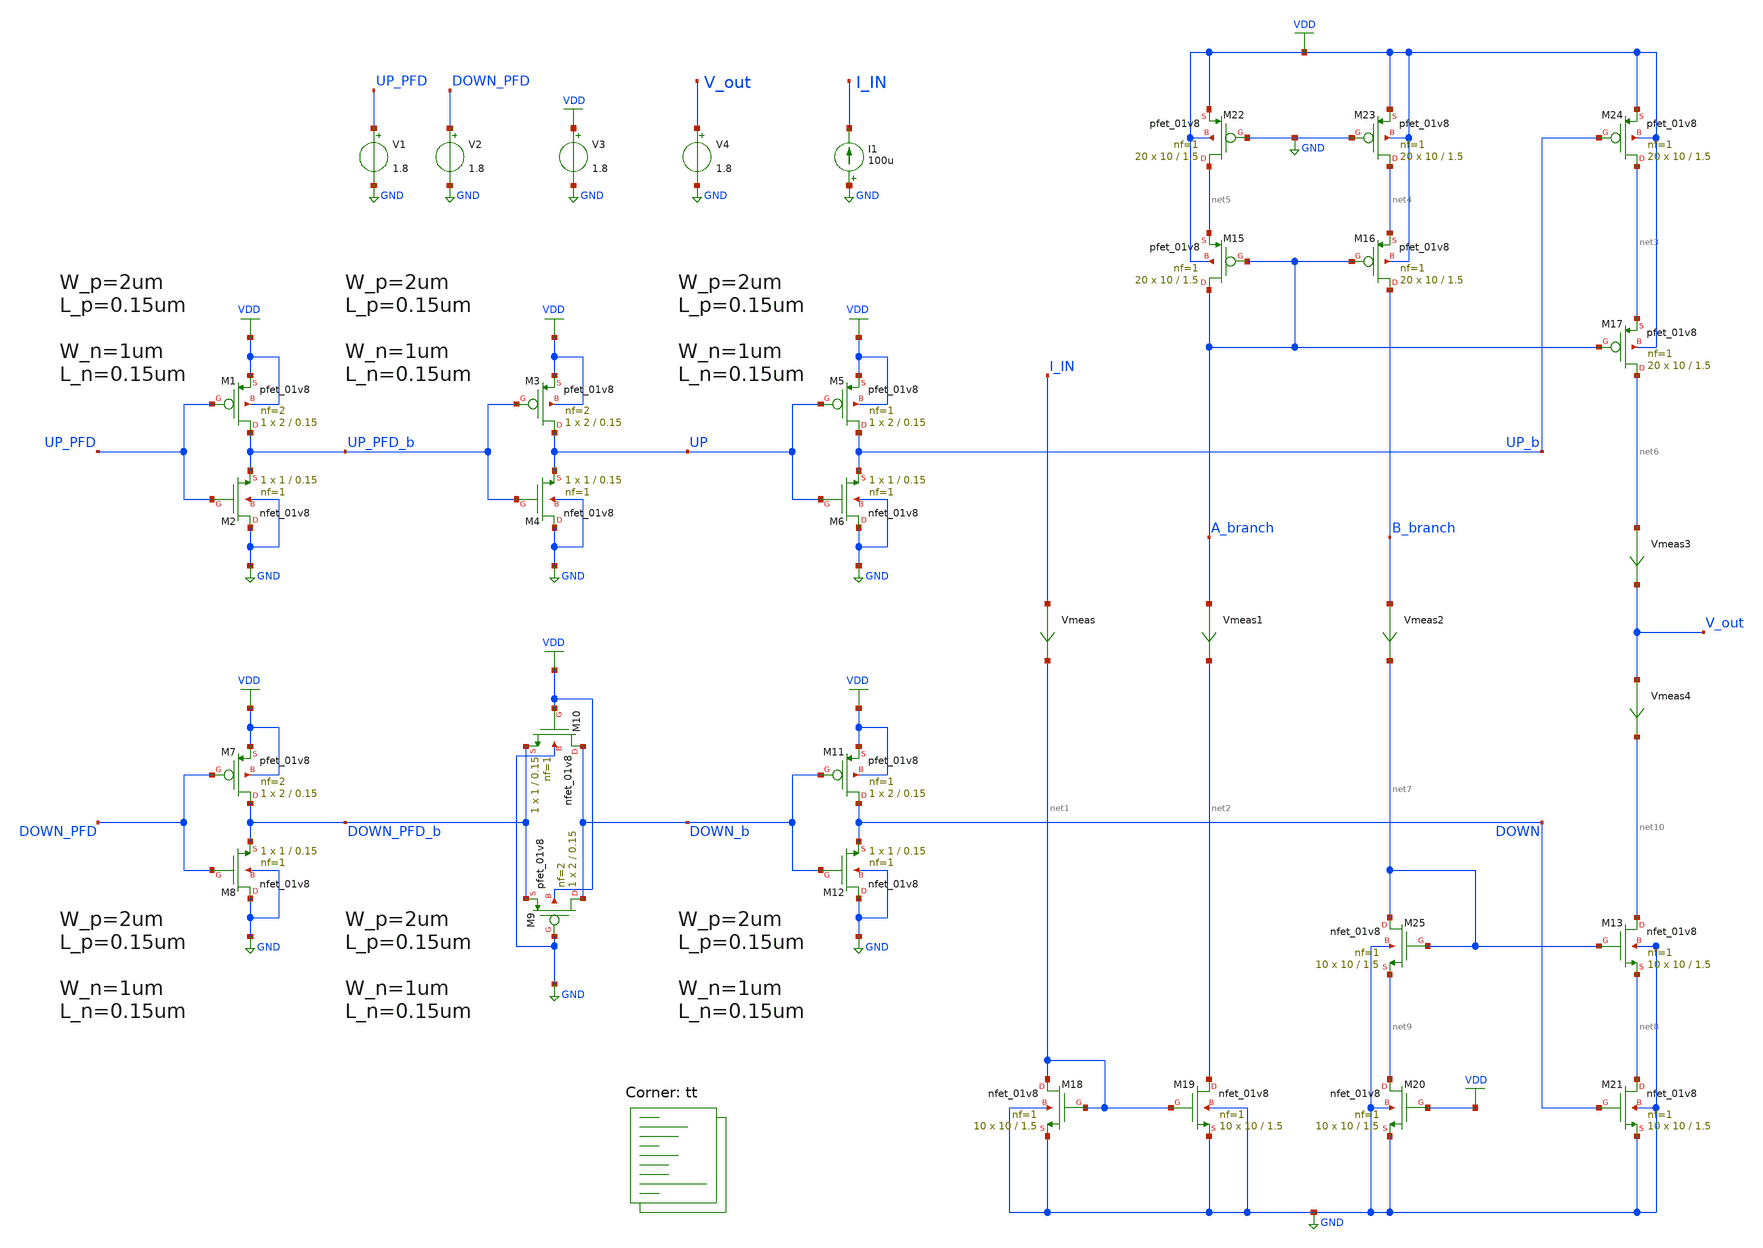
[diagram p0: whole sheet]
** sch_path: projects/pll/charge_pump/xschem_ngspice/charge_pump_DC11.sch
**.subckt charge_pump_DC11
XM9 DOWN_b GND DOWN_PFD_b VDD sky130_fd_pr__pfet_01v8 L=0.15 W=2 nf=2 ad='int((nf+1)/2) * W/nf * 0.29'
+ as='int((nf+2)/2) * W/nf * 0.29' pd='2*int((nf+1)/2) * (W/nf + 0.29)' ps='2*int((nf+2)/2) * (W/nf + 0.29)'
+ nrd='0.29 / W' nrs='0.29 / W' sa=0 sb=0 sd=0 mult=1 m=1
XM10 DOWN_b VDD DOWN_PFD_b GND sky130_fd_pr__nfet_01v8 L=0.15 W=1 nf=1 ad='int((nf+1)/2) * W/nf * 0.29'
+ as='int((nf+2)/2) * W/nf * 0.29' pd='2*int((nf+1)/2) * (W/nf + 0.29)' ps='2*int((nf+2)/2) * (W/nf + 0.29)'
+ nrd='0.29 / W' nrs='0.29 / W' sa=0 sb=0 sd=0 mult=1 m=1
XM1 UP_PFD_b UP_PFD VDD VDD sky130_fd_pr__pfet_01v8 L=0.15 W=2 nf=2 ad='int((nf+1)/2) * W/nf * 0.29'
+ as='int((nf+2)/2) * W/nf * 0.29' pd='2*int((nf+1)/2) * (W/nf + 0.29)' ps='2*int((nf+2)/2) * (W/nf + 0.29)'
+ nrd='0.29 / W' nrs='0.29 / W' sa=0 sb=0 sd=0 mult=1 m=1
XM2 GND UP_PFD UP_PFD_b GND sky130_fd_pr__nfet_01v8 L=0.15 W=1 nf=1 ad='int((nf+1)/2) * W/nf * 0.29'
+ as='int((nf+2)/2) * W/nf * 0.29' pd='2*int((nf+1)/2) * (W/nf + 0.29)' ps='2*int((nf+2)/2) * (W/nf + 0.29)'
+ nrd='0.29 / W' nrs='0.29 / W' sa=0 sb=0 sd=0 mult=1 m=1
XM7 DOWN_PFD_b DOWN_PFD VDD VDD sky130_fd_pr__pfet_01v8 L=0.15 W=2 nf=2 ad='int((nf+1)/2) * W/nf * 0.29'
+ as='int((nf+2)/2) * W/nf * 0.29' pd='2*int((nf+1)/2) * (W/nf + 0.29)' ps='2*int((nf+2)/2) * (W/nf + 0.29)'
+ nrd='0.29 / W' nrs='0.29 / W' sa=0 sb=0 sd=0 mult=1 m=1
XM8 GND DOWN_PFD DOWN_PFD_b GND sky130_fd_pr__nfet_01v8 L=0.15 W=1 nf=1 ad='int((nf+1)/2) * W/nf * 0.29'
+ as='int((nf+2)/2) * W/nf * 0.29' pd='2*int((nf+1)/2) * (W/nf + 0.29)' ps='2*int((nf+2)/2) * (W/nf + 0.29)'
+ nrd='0.29 / W' nrs='0.29 / W' sa=0 sb=0 sd=0 mult=1 m=1
XM3 UP UP_PFD_b VDD VDD sky130_fd_pr__pfet_01v8 L=0.15 W=2 nf=2 ad='int((nf+1)/2) * W/nf * 0.29' as='int((nf+2)/2) * W/nf * 0.29'
+ pd='2*int((nf+1)/2) * (W/nf + 0.29)' ps='2*int((nf+2)/2) * (W/nf + 0.29)' nrd='0.29 / W' nrs='0.29 / W'
+ sa=0 sb=0 sd=0 mult=1 m=1
XM4 GND UP_PFD_b UP GND sky130_fd_pr__nfet_01v8 L=0.15 W=1 nf=1 ad='int((nf+1)/2) * W/nf * 0.29' as='int((nf+2)/2) * W/nf * 0.29'
+ pd='2*int((nf+1)/2) * (W/nf + 0.29)' ps='2*int((nf+2)/2) * (W/nf + 0.29)' nrd='0.29 / W' nrs='0.29 / W'
+ sa=0 sb=0 sd=0 mult=1 m=1
V3 VDD GND 1.8
I1 GND I_IN 100u
V1 UP_PFD GND 1.8
V2 DOWN_PFD GND 1.8
V4 V_out GND 1.8
XM5 UP_b UP VDD VDD sky130_fd_pr__pfet_01v8 L=0.15 W=2 nf=1 ad='int((nf+1)/2) * W/nf * 0.29' as='int((nf+2)/2) * W/nf * 0.29'
+ pd='2*int((nf+1)/2) * (W/nf + 0.29)' ps='2*int((nf+2)/2) * (W/nf + 0.29)' nrd='0.29 / W' nrs='0.29 / W'
+ sa=0 sb=0 sd=0 mult=1 m=1
XM6 GND UP UP_b GND sky130_fd_pr__nfet_01v8 L=0.15 W=1 nf=1 ad='int((nf+1)/2) * W/nf * 0.29' as='int((nf+2)/2) * W/nf * 0.29'
+ pd='2*int((nf+1)/2) * (W/nf + 0.29)' ps='2*int((nf+2)/2) * (W/nf + 0.29)' nrd='0.29 / W' nrs='0.29 / W'
+ sa=0 sb=0 sd=0 mult=1 m=1
XM11 DOWN DOWN_b VDD VDD sky130_fd_pr__pfet_01v8 L=0.15 W=2 nf=1 ad='int((nf+1)/2) * W/nf * 0.29' as='int((nf+2)/2) * W/nf * 0.29'
+ pd='2*int((nf+1)/2) * (W/nf + 0.29)' ps='2*int((nf+2)/2) * (W/nf + 0.29)' nrd='0.29 / W' nrs='0.29 / W'
+ sa=0 sb=0 sd=0 mult=1 m=1
XM12 GND DOWN_b DOWN GND sky130_fd_pr__nfet_01v8 L=0.15 W=1 nf=1 ad='int((nf+1)/2) * W/nf * 0.29' as='int((nf+2)/2) * W/nf * 0.29'
+ pd='2*int((nf+1)/2) * (W/nf + 0.29)' ps='2*int((nf+2)/2) * (W/nf + 0.29)' nrd='0.29 / W' nrs='0.29 / W'
+ sa=0 sb=0 sd=0 mult=1 m=1
XM18 net1 net1 GND GND sky130_fd_pr__nfet_01v8 L=1.5 W=10 nf=1 ad='int((nf+1)/2) * W/nf * 0.29' as='int((nf+2)/2) * W/nf * 0.29'
+ pd='2*int((nf+1)/2) * (W/nf + 0.29)' ps='2*int((nf+2)/2) * (W/nf + 0.29)' nrd='0.29 / W' nrs='0.29 / W'
+ sa=0 sb=0 sd=0 mult=10 m=10
XM19 net2 net1 GND GND sky130_fd_pr__nfet_01v8 L=1.5 W=10 nf=1 ad='int((nf+1)/2) * W/nf * 0.29' as='int((nf+2)/2) * W/nf * 0.29'
+ pd='2*int((nf+1)/2) * (W/nf + 0.29)' ps='2*int((nf+2)/2) * (W/nf + 0.29)' nrd='0.29 / W' nrs='0.29 / W'
+ sa=0 sb=0 sd=0 mult=10 m=10
Vmeas I_IN net1 0
.save i(vmeas)
Vmeas3 net6 V_out 0
.save i(vmeas3)
Vmeas4 V_out net10 0
.save i(vmeas4)
XM17 net6 A_branch net3 VDD sky130_fd_pr__pfet_01v8 L=1.5 W=10 nf=1 ad='int((nf+1)/2) * W/nf * 0.29'
+ as='int((nf+2)/2) * W/nf * 0.29' pd='2*int((nf+1)/2) * (W/nf + 0.29)' ps='2*int((nf+2)/2) * (W/nf + 0.29)'
+ nrd='0.29 / W' nrs='0.29 / W' sa=0 sb=0 sd=0 mult=20 m=20
XM21 net8 DOWN GND GND sky130_fd_pr__nfet_01v8 L=1.5 W=10 nf=1 ad='int((nf+1)/2) * W/nf * 0.29' as='int((nf+2)/2) * W/nf * 0.29'
+ pd='2*int((nf+1)/2) * (W/nf + 0.29)' ps='2*int((nf+2)/2) * (W/nf + 0.29)' nrd='0.29 / W' nrs='0.29 / W'
+ sa=0 sb=0 sd=0 mult=10 m=10
XM20 net9 VDD GND GND sky130_fd_pr__nfet_01v8 L=1.5 W=10 nf=1 ad='int((nf+1)/2) * W/nf * 0.29' as='int((nf+2)/2) * W/nf * 0.29'
+ pd='2*int((nf+1)/2) * (W/nf + 0.29)' ps='2*int((nf+2)/2) * (W/nf + 0.29)' nrd='0.29 / W' nrs='0.29 / W'
+ sa=0 sb=0 sd=0 mult=10 m=10
XM15 A_branch A_branch net5 VDD sky130_fd_pr__pfet_01v8 L=1.5 W=10 nf=1 ad='int((nf+1)/2) * W/nf * 0.29'
+ as='int((nf+2)/2) * W/nf * 0.29' pd='2*int((nf+1)/2) * (W/nf + 0.29)' ps='2*int((nf+2)/2) * (W/nf + 0.29)'
+ nrd='0.29 / W' nrs='0.29 / W' sa=0 sb=0 sd=0 mult=20 m=20
XM16 B_branch A_branch net4 VDD sky130_fd_pr__pfet_01v8 L=1.5 W=10 nf=1 ad='int((nf+1)/2) * W/nf * 0.29'
+ as='int((nf+2)/2) * W/nf * 0.29' pd='2*int((nf+1)/2) * (W/nf + 0.29)' ps='2*int((nf+2)/2) * (W/nf + 0.29)'
+ nrd='0.29 / W' nrs='0.29 / W' sa=0 sb=0 sd=0 mult=20 m=20
Vmeas1 A_branch net2 0
.save i(vmeas1)
Vmeas2 B_branch net7 0
.save i(vmeas2)
XM22 net5 GND VDD VDD sky130_fd_pr__pfet_01v8 L=1.5 W=10 nf=1 ad='int((nf+1)/2) * W/nf * 0.29' as='int((nf+2)/2) * W/nf * 0.29'
+ pd='2*int((nf+1)/2) * (W/nf + 0.29)' ps='2*int((nf+2)/2) * (W/nf + 0.29)' nrd='0.29 / W' nrs='0.29 / W'
+ sa=0 sb=0 sd=0 mult=20 m=20
XM23 net4 GND VDD VDD sky130_fd_pr__pfet_01v8 L=1.5 W=10 nf=1 ad='int((nf+1)/2) * W/nf * 0.29' as='int((nf+2)/2) * W/nf * 0.29'
+ pd='2*int((nf+1)/2) * (W/nf + 0.29)' ps='2*int((nf+2)/2) * (W/nf + 0.29)' nrd='0.29 / W' nrs='0.29 / W'
+ sa=0 sb=0 sd=0 mult=20 m=20
XM24 net3 UP_b VDD VDD sky130_fd_pr__pfet_01v8 L=1.5 W=10 nf=1 ad='int((nf+1)/2) * W/nf * 0.29' as='int((nf+2)/2) * W/nf * 0.29'
+ pd='2*int((nf+1)/2) * (W/nf + 0.29)' ps='2*int((nf+2)/2) * (W/nf + 0.29)' nrd='0.29 / W' nrs='0.29 / W'
+ sa=0 sb=0 sd=0 mult=20 m=20
XM13 net10 net7 net8 GND sky130_fd_pr__nfet_01v8 L=1.5 W=10 nf=1 ad='int((nf+1)/2) * W/nf * 0.29' as='int((nf+2)/2) * W/nf * 0.29'
+ pd='2*int((nf+1)/2) * (W/nf + 0.29)' ps='2*int((nf+2)/2) * (W/nf + 0.29)' nrd='0.29 / W' nrs='0.29 / W'
+ sa=0 sb=0 sd=0 mult=10 m=10
XM25 net7 net7 net9 GND sky130_fd_pr__nfet_01v8 L=1.5 W=10 nf=1 ad='int((nf+1)/2) * W/nf * 0.29' as='int((nf+2)/2) * W/nf * 0.29'
+ pd='2*int((nf+1)/2) * (W/nf + 0.29)' ps='2*int((nf+2)/2) * (W/nf + 0.29)' nrd='0.29 / W' nrs='0.29 / W'
+ sa=0 sb=0 sd=0 mult=10 m=10
**** begin user architecture code
.lib $::SKYWATER_MODELS/sky130.lib.spice tt



.option method=gear
.option wnflag=1

.control
  save all
  dc v4 0 1.8 0.01 v1 0 1.8 1.8
  remzerovec
  write charge_pump_DC11.raw
  set appendwrite
.endc



**** end user architecture code
**.ends
.GLOBAL VDD
.GLOBAL GND
.end
